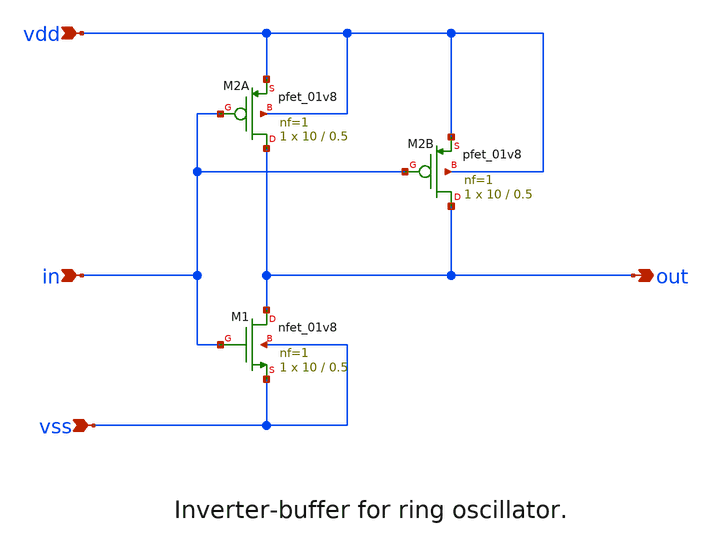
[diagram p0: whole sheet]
** sch_path: xschem/ringosc_buf.sch
**.subckt ringosc_buf vdd vss in out
*.ipin vdd
*.ipin vss
*.ipin in
*.opin out
XM1 out in vss vss sky130_fd_pr__nfet_01v8 L=0.5 W=10 nf=1 ad='int((nf+1)/2) * W/nf * 0.29' as='int((nf+2)/2) * W/nf * 0.29'
+ pd='2*int((nf+1)/2) * (W/nf + 0.29)' ps='2*int((nf+2)/2) * (W/nf + 0.29)' nrd='0.29 / W' nrs='0.29 / W'
+ sa=0 sb=0 sd=0 mult=1 m=1
XM2A out in vdd vdd sky130_fd_pr__pfet_01v8 L=0.5 W=10 nf=1 ad='int((nf+1)/2) * W/nf * 0.29' as='int((nf+2)/2) * W/nf * 0.29'
+ pd='2*int((nf+1)/2) * (W/nf + 0.29)' ps='2*int((nf+2)/2) * (W/nf + 0.29)' nrd='0.29 / W' nrs='0.29 / W'
+ sa=0 sb=0 sd=0 mult=1 m=1
XM2B out in vdd vdd sky130_fd_pr__pfet_01v8 L=0.5 W=10 nf=1 ad='int((nf+1)/2) * W/nf * 0.29' as='int((nf+2)/2) * W/nf * 0.29'
+ pd='2*int((nf+1)/2) * (W/nf + 0.29)' ps='2*int((nf+2)/2) * (W/nf + 0.29)' nrd='0.29 / W' nrs='0.29 / W'
+ sa=0 sb=0 sd=0 mult=1 m=1
**.ends
.end
